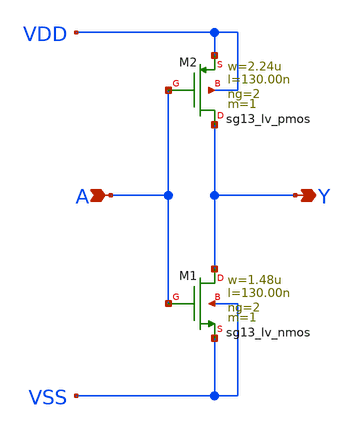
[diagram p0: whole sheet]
** sch_path: ihp-sg13g2/libs.ref/sg13g2_stdcell/sch/xschem/sg13g2_inv_2.sch
* Copyright 2023 IHP PDK Authors
* Licensed under the Apache License, Version 2.0 (the "License");
* you may not use this file except in compliance with the License.
* You may obtain a copy of the License at
* https://www.apache.org/licenses/LICENSE-2.0
* Unless required by applicable law or agreed to in writing, software
* distributed under the License is distributed on an "AS IS" BASIS,
* WITHOUT WARRANTIES OR CONDITIONS OF ANY KIND, either express or implied.
* See the License for the specific language governing permissions and
* limitations under the License.
**.subckt sg13g2_inv_2 Y A
*.opin Y
*.ipin A
XM1 Y A VSS VSS sg13_lv_nmos w=1.48u l=130.00n ng=2 m=1 mm_ok=1
XM2 Y A VDD VDD sg13_lv_pmos w=2.24u l=130.00n ng=2 m=1 mm_ok=1
**.ends
.end
